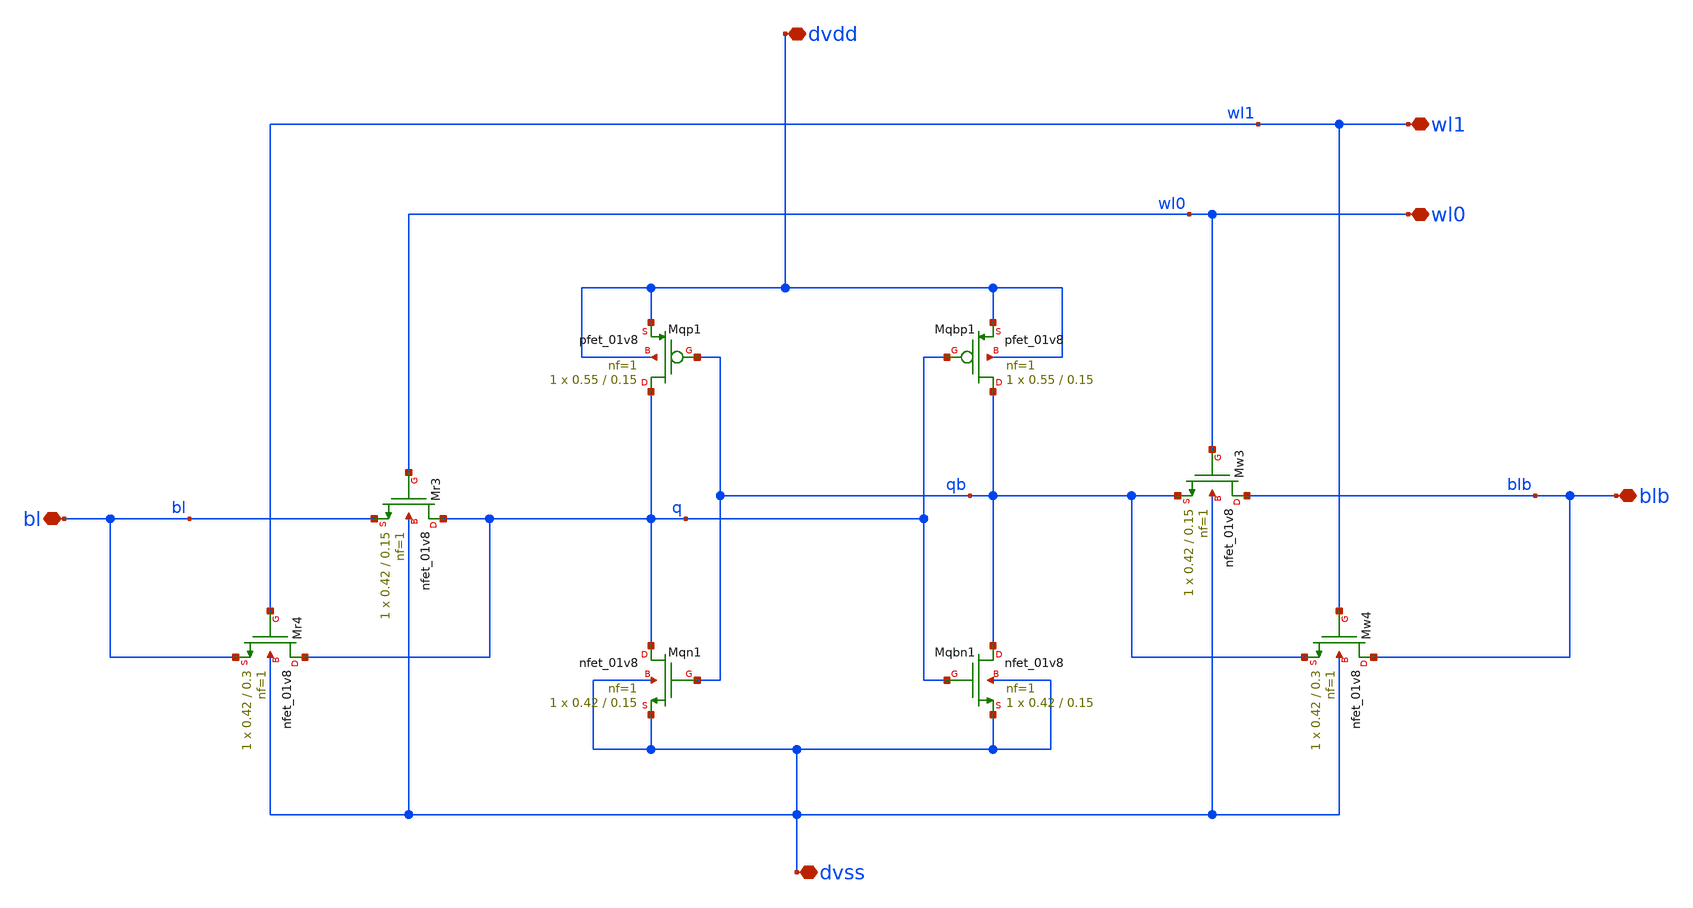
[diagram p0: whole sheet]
** sch_path: 8T_SRAM_cell.sch
**.subckt 8T_SRAM_cell dvdd dvss bl blb wl1 wl0
*.iopin dvdd
*.iopin dvss
*.iopin bl
*.iopin blb
*.iopin wl1
*.iopin wl0
XMqbn1 qb q dvss dvss sky130_fd_pr__nfet_01v8 L=0.15 W=0.42 nf=1 ad='int((1 + 1)/2) * 0.42 / 1 * 0.29'
+ as='int((1 + 2)/2) * 0.42 / 1 * 0.29' pd='2*int((1 + 1)/2) * (0.42 / 1 + 0.29)' ps='2*int((1 + 2)/2) * (0.42 / 1 + 0.29)'
+ nrd='0.29 / 0.42 ' nrs='0.29 / 0.42 ' sa=0 sb=0 sd=0 mult=1 m=1
XMqn1 q qb dvss dvss sky130_fd_pr__nfet_01v8 L=0.15 W=0.42 nf=1 ad='int((1 + 1)/2) * 0.42 / 1 * 0.29'
+ as='int((1 + 2)/2) * 0.42 / 1 * 0.29' pd='2*int((1 + 1)/2) * (0.42 / 1 + 0.29)' ps='2*int((1 + 2)/2) * (0.42 / 1 + 0.29)'
+ nrd='0.29 / 0.42 ' nrs='0.29 / 0.42 ' sa=0 sb=0 sd=0 mult=1 m=1
XMr3 q wl0 bl dvss sky130_fd_pr__nfet_01v8 L=0.15 W=0.42 nf=1 ad='int((1 + 1)/2) * 0.42 / 1 * 0.29' as='int((1 + 2)/2) * 0.42 / 1 * 0.29'
+ pd='2*int((1 + 1)/2) * (0.42 / 1 + 0.29)' ps='2*int((1 + 2)/2) * (0.42 / 1 + 0.29)' nrd='0.29 / 0.42 '
+ nrs='0.29 / 0.42 ' sa=0 sb=0 sd=0 mult=1 m=1
XMr4 q wl1 bl dvss sky130_fd_pr__nfet_01v8 L=0.3 W=0.42 nf=1 ad='int((1 + 1)/2) * 0.42 / 1 * 0.29' as='int((1 + 2)/2) * 0.42 / 1 * 0.29'
+ pd='2*int((1 + 1)/2) * (0.42 / 1 + 0.29)' ps='2*int((1 + 2)/2) * (0.42 / 1 + 0.29)' nrd='0.29 / 0.42 '
+ nrs='0.29 / 0.42 ' sa=0 sb=0 sd=0 mult=1 m=1
XMw3 blb wl0 qb dvss sky130_fd_pr__nfet_01v8 L=0.15 W=0.42 nf=1 ad='int((1 + 1)/2) * 0.42 / 1 * 0.29'
+ as='int((1 + 2)/2) * 0.42 / 1 * 0.29' pd='2*int((1 + 1)/2) * (0.42 / 1 + 0.29)' ps='2*int((1 + 2)/2) * (0.42 / 1 + 0.29)'
+ nrd='0.29 / 0.42 ' nrs='0.29 / 0.42 ' sa=0 sb=0 sd=0 mult=1 m=1
XMw4 blb wl1 qb dvss sky130_fd_pr__nfet_01v8 L=0.3 W=0.42 nf=1 ad='int((1 + 1)/2) * 0.42 / 1 * 0.29'
+ as='int((1 + 2)/2) * 0.42 / 1 * 0.29' pd='2*int((1 + 1)/2) * (0.42 / 1 + 0.29)' ps='2*int((1 + 2)/2) * (0.42 / 1 + 0.29)'
+ nrd='0.29 / 0.42 ' nrs='0.29 / 0.42 ' sa=0 sb=0 sd=0 mult=1 m=1
XMqp1 q qb dvdd dvdd sky130_fd_pr__pfet_01v8 L=0.15 W=0.55 nf=1 ad='int((1 + 1)/2) * 0.55 / 1 * 0.29'
+ as='int((1 + 2)/2) * 0.55 / 1 * 0.29' pd='2*int((1 + 1)/2) * (0.55 / 1 + 0.29)' ps='2*int((1 + 2)/2) * (0.55 / 1 + 0.29)'
+ nrd='0.29 / 0.55 ' nrs='0.29 / 0.55 ' sa=0 sb=0 sd=0 mult=1 m=1
XMqbp1 qb q dvdd dvdd sky130_fd_pr__pfet_01v8 L=0.15 W=0.55 nf=1 ad='int((1 + 1)/2) * 0.55 / 1 * 0.29'
+ as='int((1 + 2)/2) * 0.55 / 1 * 0.29' pd='2*int((1 + 1)/2) * (0.55 / 1 + 0.29)' ps='2*int((1 + 2)/2) * (0.55 / 1 + 0.29)'
+ nrd='0.29 / 0.55 ' nrs='0.29 / 0.55 ' sa=0 sb=0 sd=0 mult=1 m=1
**** begin user architecture code
.lib /usr/local/share/pdk/sky130A/libs.tech/ngspice/sky130.lib.spice tt
**** end user architecture code
**.ends
.end
